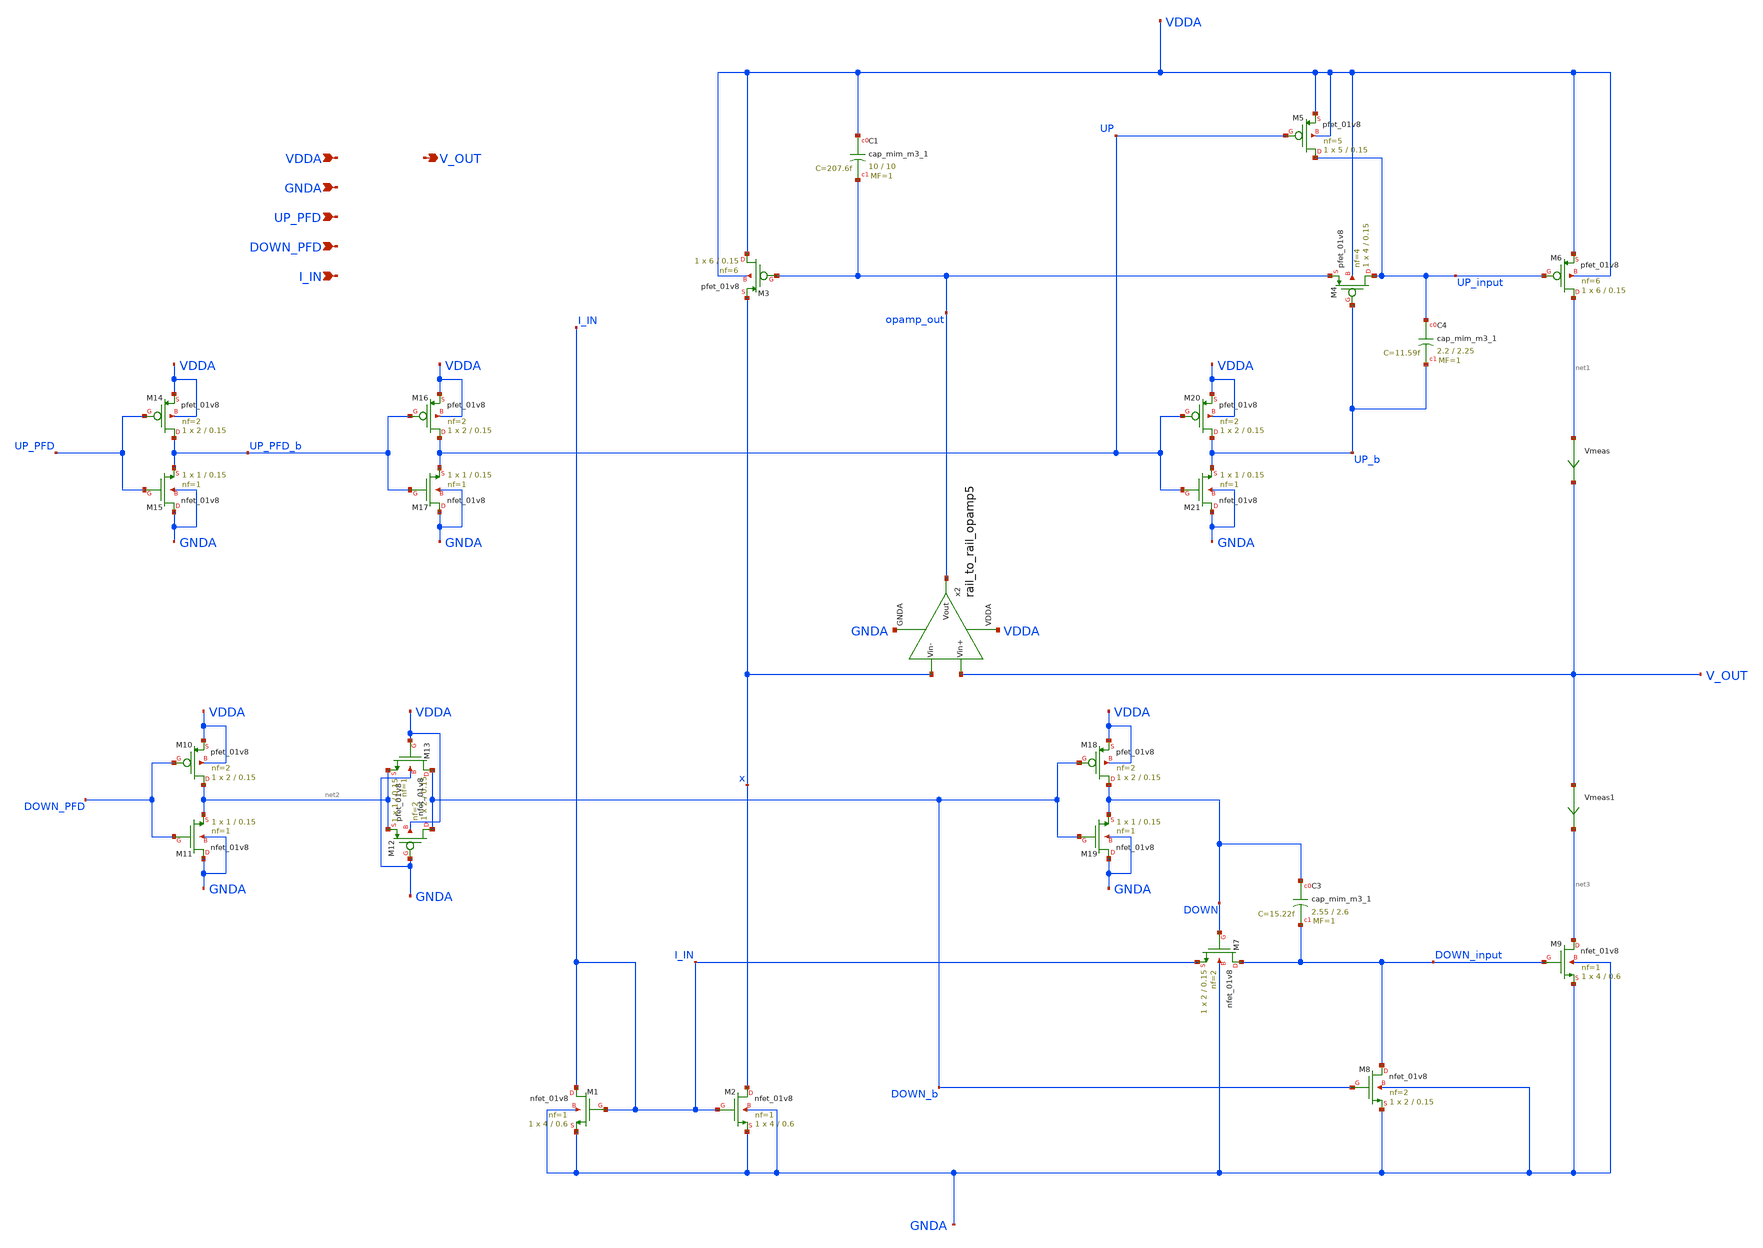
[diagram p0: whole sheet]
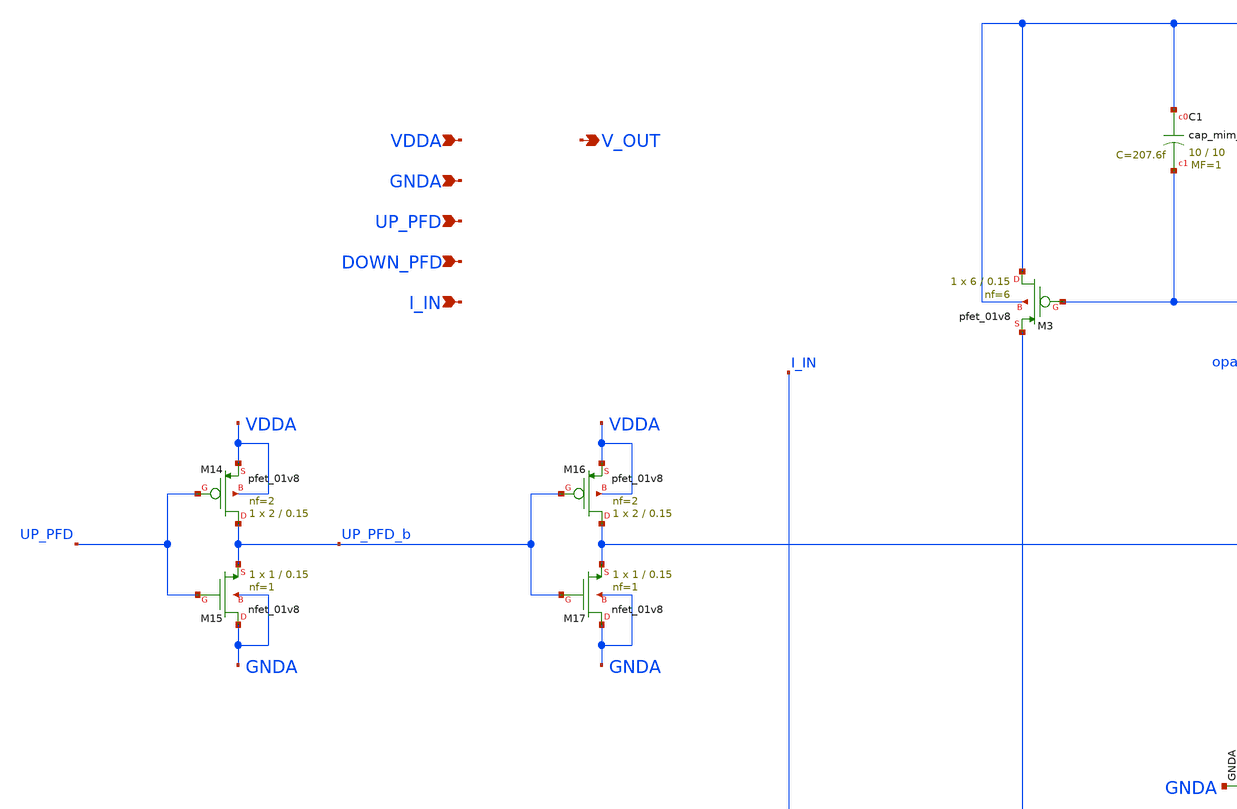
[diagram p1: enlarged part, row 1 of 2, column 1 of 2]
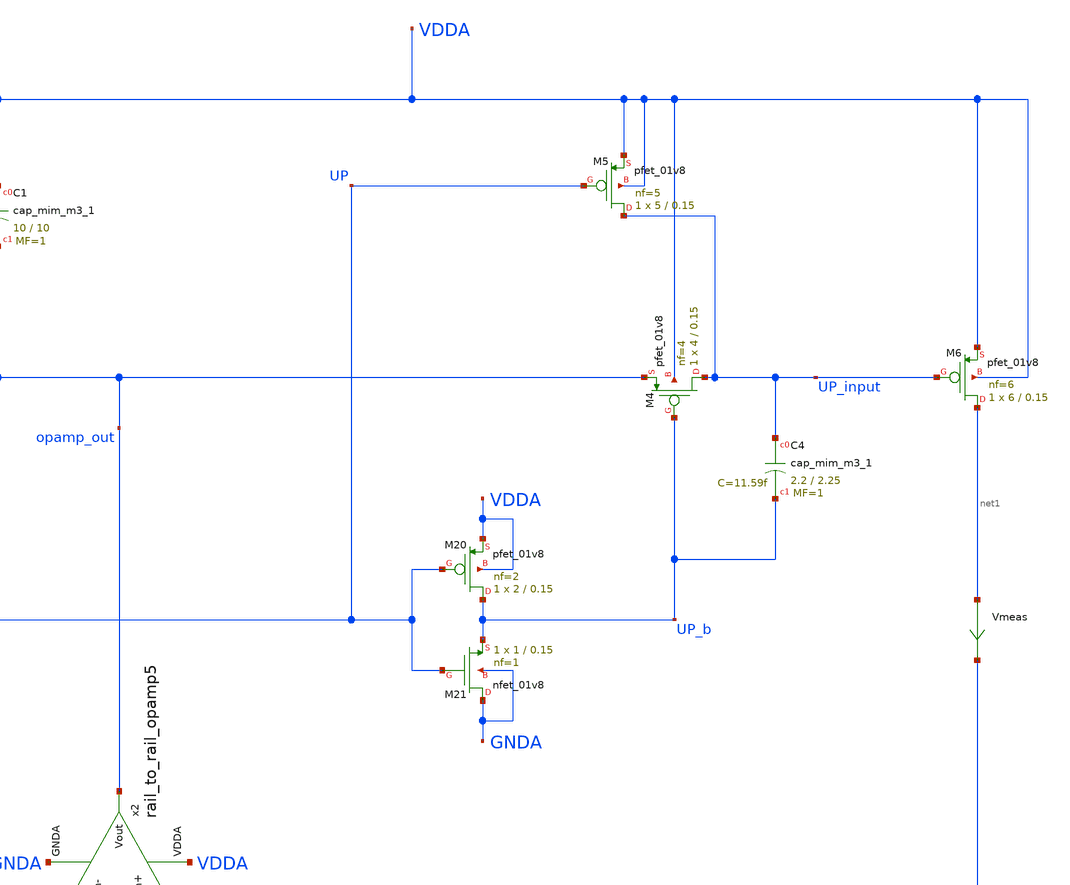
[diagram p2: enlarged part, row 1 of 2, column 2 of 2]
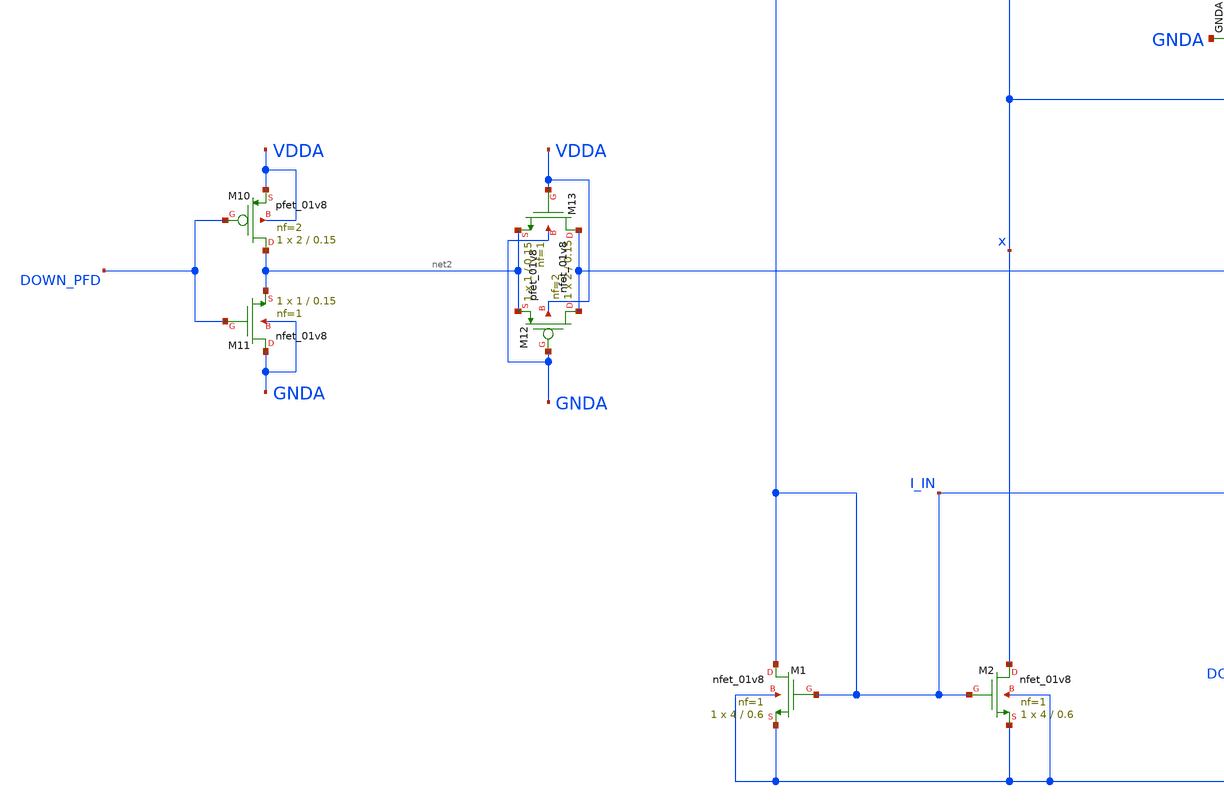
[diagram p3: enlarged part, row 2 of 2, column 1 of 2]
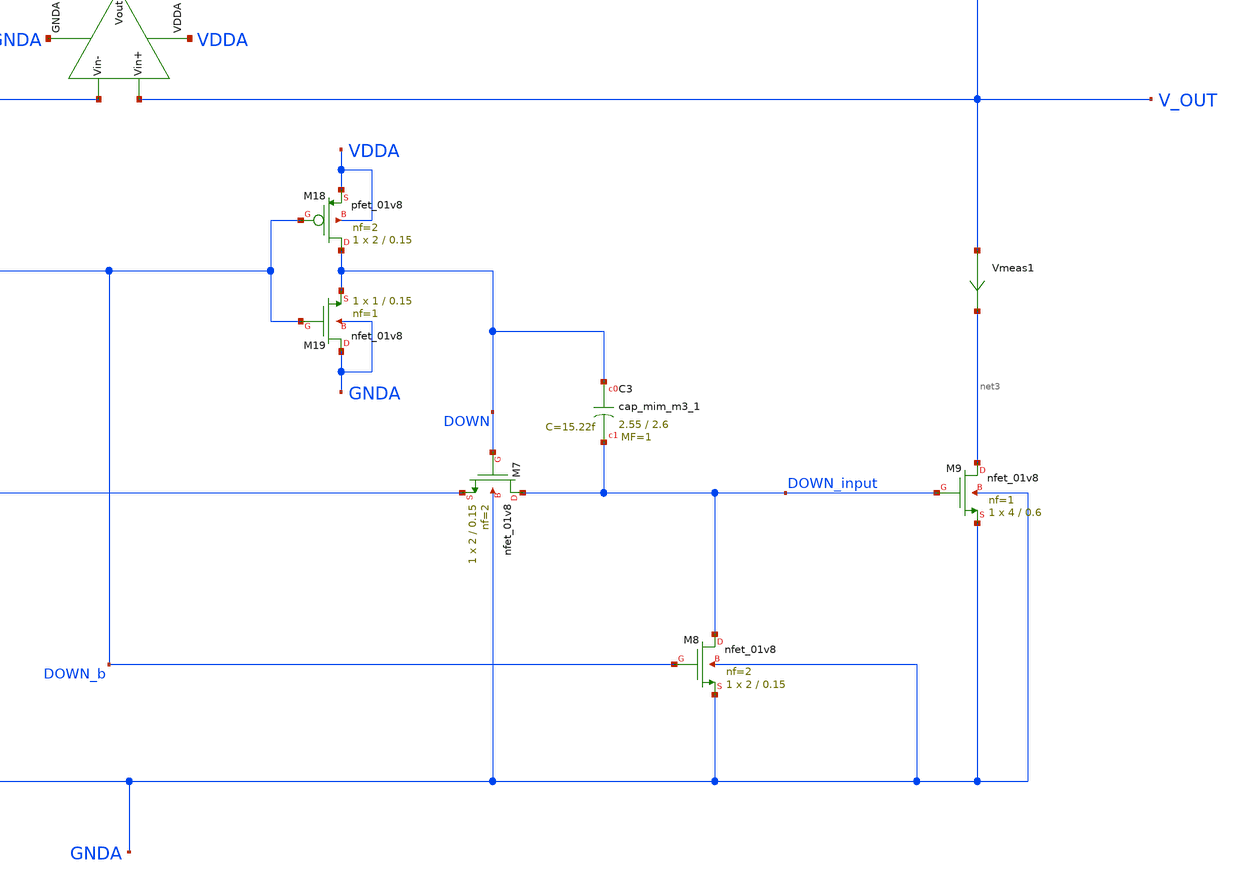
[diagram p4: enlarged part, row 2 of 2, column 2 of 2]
** sch_path: projects/pll/charge_pump/xschem_ngspice/charge_pump5.sch
**.subckt charge_pump5 VDDA V_OUT GNDA UP_PFD DOWN_PFD I_IN
*.ipin VDDA
*.opin V_OUT
*.ipin GNDA
*.ipin UP_PFD
*.ipin DOWN_PFD
*.ipin I_IN
XM1 I_IN I_IN GNDA GNDA sky130_fd_pr__nfet_01v8 L=0.6 W=4 nf=1 ad='int((nf+1)/2) * W/nf * 0.29' as='int((nf+2)/2) * W/nf * 0.29'
+ pd='2*int((nf+1)/2) * (W/nf + 0.29)' ps='2*int((nf+2)/2) * (W/nf + 0.29)' nrd='0.29 / W' nrs='0.29 / W'
+ sa=0 sb=0 sd=0 mult=1 m=1
XM2 x I_IN GNDA GNDA sky130_fd_pr__nfet_01v8 L=0.6 W=4 nf=1 ad='int((nf+1)/2) * W/nf * 0.29' as='int((nf+2)/2) * W/nf * 0.29'
+ pd='2*int((nf+1)/2) * (W/nf + 0.29)' ps='2*int((nf+2)/2) * (W/nf + 0.29)' nrd='0.29 / W' nrs='0.29 / W'
+ sa=0 sb=0 sd=0 mult=1 m=1
XM3 VDDA opamp_out x VDDA sky130_fd_pr__pfet_01v8 L=0.15 W=6 nf=6 ad='int((nf+1)/2) * W/nf * 0.29' as='int((nf+2)/2) * W/nf * 0.29'
+ pd='2*int((nf+1)/2) * (W/nf + 0.29)' ps='2*int((nf+2)/2) * (W/nf + 0.29)' nrd='0.29 / W' nrs='0.29 / W'
+ sa=0 sb=0 sd=0 mult=1 m=1
XM4 UP_input UP_b opamp_out VDDA sky130_fd_pr__pfet_01v8 L=0.15 W=4 nf=4 ad='int((nf+1)/2) * W/nf * 0.29'
+ as='int((nf+2)/2) * W/nf * 0.29' pd='2*int((nf+1)/2) * (W/nf + 0.29)' ps='2*int((nf+2)/2) * (W/nf + 0.29)'
+ nrd='0.29 / W' nrs='0.29 / W' sa=0 sb=0 sd=0 mult=1 m=1
XM5 UP_input UP VDDA VDDA sky130_fd_pr__pfet_01v8 L=0.15 W=5 nf=5 ad='int((nf+1)/2) * W/nf * 0.29' as='int((nf+2)/2) * W/nf * 0.29'
+ pd='2*int((nf+1)/2) * (W/nf + 0.29)' ps='2*int((nf+2)/2) * (W/nf + 0.29)' nrd='0.29 / W' nrs='0.29 / W'
+ sa=0 sb=0 sd=0 mult=1 m=1
XM6 net1 UP_input VDDA VDDA sky130_fd_pr__pfet_01v8 L=0.15 W=6 nf=6 ad='int((nf+1)/2) * W/nf * 0.29'
+ as='int((nf+2)/2) * W/nf * 0.29' pd='2*int((nf+1)/2) * (W/nf + 0.29)' ps='2*int((nf+2)/2) * (W/nf + 0.29)'
+ nrd='0.29 / W' nrs='0.29 / W' sa=0 sb=0 sd=0 mult=1 m=1
XM7 DOWN_input DOWN I_IN GNDA sky130_fd_pr__nfet_01v8 L=0.15 W=2 nf=2 ad='int((nf+1)/2) * W/nf * 0.29'
+ as='int((nf+2)/2) * W/nf * 0.29' pd='2*int((nf+1)/2) * (W/nf + 0.29)' ps='2*int((nf+2)/2) * (W/nf + 0.29)'
+ nrd='0.29 / W' nrs='0.29 / W' sa=0 sb=0 sd=0 mult=1 m=1
XM8 DOWN_input DOWN_b GNDA GNDA sky130_fd_pr__nfet_01v8 L=0.15 W=2 nf=2 ad='int((nf+1)/2) * W/nf * 0.29'
+ as='int((nf+2)/2) * W/nf * 0.29' pd='2*int((nf+1)/2) * (W/nf + 0.29)' ps='2*int((nf+2)/2) * (W/nf + 0.29)'
+ nrd='0.29 / W' nrs='0.29 / W' sa=0 sb=0 sd=0 mult=1 m=1
XM9 net3 DOWN_input GNDA GNDA sky130_fd_pr__nfet_01v8 L=0.6 W=4 nf=1 ad='int((nf+1)/2) * W/nf * 0.29'
+ as='int((nf+2)/2) * W/nf * 0.29' pd='2*int((nf+1)/2) * (W/nf + 0.29)' ps='2*int((nf+2)/2) * (W/nf + 0.29)'
+ nrd='0.29 / W' nrs='0.29 / W' sa=0 sb=0 sd=0 mult=1 m=1
x2 VDDA V_OUT x opamp_out GNDA rail_to_rail_opamp5
XM12 DOWN_b GNDA net2 VDDA sky130_fd_pr__pfet_01v8 L=0.15 W=2 nf=2 ad='int((nf+1)/2) * W/nf * 0.29' as='int((nf+2)/2) * W/nf * 0.29'
+ pd='2*int((nf+1)/2) * (W/nf + 0.29)' ps='2*int((nf+2)/2) * (W/nf + 0.29)' nrd='0.29 / W' nrs='0.29 / W'
+ sa=0 sb=0 sd=0 mult=1 m=1
XM13 DOWN_b VDDA net2 GNDA sky130_fd_pr__nfet_01v8 L=0.15 W=1 nf=1 ad='int((nf+1)/2) * W/nf * 0.29' as='int((nf+2)/2) * W/nf * 0.29'
+ pd='2*int((nf+1)/2) * (W/nf + 0.29)' ps='2*int((nf+2)/2) * (W/nf + 0.29)' nrd='0.29 / W' nrs='0.29 / W'
+ sa=0 sb=0 sd=0 mult=1 m=1
XC3 DOWN DOWN_input sky130_fd_pr__cap_mim_m3_1 W=2.55 L=2.6 MF=1 m=1
XC4 UP_input UP_b sky130_fd_pr__cap_mim_m3_1 W=2.2 L=2.25 MF=1 m=1
XM10 net2 DOWN_PFD VDDA VDDA sky130_fd_pr__pfet_01v8 L=0.15 W=2 nf=2 ad='int((nf+1)/2) * W/nf * 0.29'
+ as='int((nf+2)/2) * W/nf * 0.29' pd='2*int((nf+1)/2) * (W/nf + 0.29)' ps='2*int((nf+2)/2) * (W/nf + 0.29)'
+ nrd='0.29 / W' nrs='0.29 / W' sa=0 sb=0 sd=0 mult=1 m=1
XM11 GNDA DOWN_PFD net2 GNDA sky130_fd_pr__nfet_01v8 L=0.15 W=1 nf=1 ad='int((nf+1)/2) * W/nf * 0.29'
+ as='int((nf+2)/2) * W/nf * 0.29' pd='2*int((nf+1)/2) * (W/nf + 0.29)' ps='2*int((nf+2)/2) * (W/nf + 0.29)'
+ nrd='0.29 / W' nrs='0.29 / W' sa=0 sb=0 sd=0 mult=1 m=1
XM14 UP_PFD_b UP_PFD VDDA VDDA sky130_fd_pr__pfet_01v8 L=0.15 W=2 nf=2 ad='int((nf+1)/2) * W/nf * 0.29'
+ as='int((nf+2)/2) * W/nf * 0.29' pd='2*int((nf+1)/2) * (W/nf + 0.29)' ps='2*int((nf+2)/2) * (W/nf + 0.29)'
+ nrd='0.29 / W' nrs='0.29 / W' sa=0 sb=0 sd=0 mult=1 m=1
XM15 GNDA UP_PFD UP_PFD_b GNDA sky130_fd_pr__nfet_01v8 L=0.15 W=1 nf=1 ad='int((nf+1)/2) * W/nf * 0.29'
+ as='int((nf+2)/2) * W/nf * 0.29' pd='2*int((nf+1)/2) * (W/nf + 0.29)' ps='2*int((nf+2)/2) * (W/nf + 0.29)'
+ nrd='0.29 / W' nrs='0.29 / W' sa=0 sb=0 sd=0 mult=1 m=1
XM16 UP UP_PFD_b VDDA VDDA sky130_fd_pr__pfet_01v8 L=0.15 W=2 nf=2 ad='int((nf+1)/2) * W/nf * 0.29' as='int((nf+2)/2) * W/nf * 0.29'
+ pd='2*int((nf+1)/2) * (W/nf + 0.29)' ps='2*int((nf+2)/2) * (W/nf + 0.29)' nrd='0.29 / W' nrs='0.29 / W'
+ sa=0 sb=0 sd=0 mult=1 m=1
XM17 GNDA UP_PFD_b UP GNDA sky130_fd_pr__nfet_01v8 L=0.15 W=1 nf=1 ad='int((nf+1)/2) * W/nf * 0.29' as='int((nf+2)/2) * W/nf * 0.29'
+ pd='2*int((nf+1)/2) * (W/nf + 0.29)' ps='2*int((nf+2)/2) * (W/nf + 0.29)' nrd='0.29 / W' nrs='0.29 / W'
+ sa=0 sb=0 sd=0 mult=1 m=1
XM18 DOWN DOWN_b VDDA VDDA sky130_fd_pr__pfet_01v8 L=0.15 W=2 nf=2 ad='int((nf+1)/2) * W/nf * 0.29' as='int((nf+2)/2) * W/nf * 0.29'
+ pd='2*int((nf+1)/2) * (W/nf + 0.29)' ps='2*int((nf+2)/2) * (W/nf + 0.29)' nrd='0.29 / W' nrs='0.29 / W'
+ sa=0 sb=0 sd=0 mult=1 m=1
XM19 GNDA DOWN_b DOWN GNDA sky130_fd_pr__nfet_01v8 L=0.15 W=1 nf=1 ad='int((nf+1)/2) * W/nf * 0.29' as='int((nf+2)/2) * W/nf * 0.29'
+ pd='2*int((nf+1)/2) * (W/nf + 0.29)' ps='2*int((nf+2)/2) * (W/nf + 0.29)' nrd='0.29 / W' nrs='0.29 / W'
+ sa=0 sb=0 sd=0 mult=1 m=1
XM20 UP_b UP VDDA VDDA sky130_fd_pr__pfet_01v8 L=0.15 W=2 nf=2 ad='int((nf+1)/2) * W/nf * 0.29' as='int((nf+2)/2) * W/nf * 0.29'
+ pd='2*int((nf+1)/2) * (W/nf + 0.29)' ps='2*int((nf+2)/2) * (W/nf + 0.29)' nrd='0.29 / W' nrs='0.29 / W'
+ sa=0 sb=0 sd=0 mult=1 m=1
XM21 GNDA UP UP_b GNDA sky130_fd_pr__nfet_01v8 L=0.15 W=1 nf=1 ad='int((nf+1)/2) * W/nf * 0.29' as='int((nf+2)/2) * W/nf * 0.29'
+ pd='2*int((nf+1)/2) * (W/nf + 0.29)' ps='2*int((nf+2)/2) * (W/nf + 0.29)' nrd='0.29 / W' nrs='0.29 / W'
+ sa=0 sb=0 sd=0 mult=1 m=1
Vmeas net1 V_OUT 0
.save i(vmeas)
Vmeas1 V_OUT net3 0
.save i(vmeas1)
XC1 VDDA opamp_out sky130_fd_pr__cap_mim_m3_1 W=10 L=10 MF=1 m=1
**.ends

* expanding   symbol:
*+  /foss/designs/my_design/projects/pll/charge_pump/xschem_ngspice/rail_to_rail_opamp5.sym # of pins=5
** sym_path: projects/pll/charge_pump/xschem_ngspice/rail_to_rail_opamp5.sym
** sch_path: projects/pll/charge_pump/xschem_ngspice/rail_to_rail_opamp5.sch
.subckt rail_to_rail_opamp5 VDDA Vin+ Vin- Vout GNDA
*.opin Vout
*.ipin Vin+
*.ipin Vin-
*.ipin VDDA
*.ipin GNDA
XM2 n_left Vin+ v_common_n GNDA sky130_fd_pr__nfet_01v8 L=0.15 W=1 nf=1 ad='int((nf+1)/2) * W/nf * 0.29'
+ as='int((nf+2)/2) * W/nf * 0.29' pd='2*int((nf+1)/2) * (W/nf + 0.29)' ps='2*int((nf+2)/2) * (W/nf + 0.29)'
+ nrd='0.29 / W' nrs='0.29 / W' sa=0 sb=0 sd=0 mult=1 m=1
XM3 n_right Vin- v_common_n GNDA sky130_fd_pr__nfet_01v8 L=0.15 W=1 nf=1 ad='int((nf+1)/2) * W/nf * 0.29'
+ as='int((nf+2)/2) * W/nf * 0.29' pd='2*int((nf+1)/2) * (W/nf + 0.29)' ps='2*int((nf+2)/2) * (W/nf + 0.29)'
+ nrd='0.29 / W' nrs='0.29 / W' sa=0 sb=0 sd=0 mult=1 m=1
XM5 n_left n_left VDDA VDDA sky130_fd_pr__pfet_01v8 L=0.15 W=2 nf=2 ad='int((nf+1)/2) * W/nf * 0.29'
+ as='int((nf+2)/2) * W/nf * 0.29' pd='2*int((nf+1)/2) * (W/nf + 0.29)' ps='2*int((nf+2)/2) * (W/nf + 0.29)'
+ nrd='0.29 / W' nrs='0.29 / W' sa=0 sb=0 sd=0 mult=1 m=1
XM4 n_right n_left VDDA VDDA sky130_fd_pr__pfet_01v8 L=0.15 W=2 nf=2 ad='int((nf+1)/2) * W/nf * 0.29'
+ as='int((nf+2)/2) * W/nf * 0.29' pd='2*int((nf+1)/2) * (W/nf + 0.29)' ps='2*int((nf+2)/2) * (W/nf + 0.29)'
+ nrd='0.29 / W' nrs='0.29 / W' sa=0 sb=0 sd=0 mult=1 m=1
XM6 v_common_p p_bias VDDA VDDA sky130_fd_pr__pfet_01v8 L=0.15 W=3 nf=3 ad='int((nf+1)/2) * W/nf * 0.29'
+ as='int((nf+2)/2) * W/nf * 0.29' pd='2*int((nf+1)/2) * (W/nf + 0.29)' ps='2*int((nf+2)/2) * (W/nf + 0.29)'
+ nrd='0.29 / W' nrs='0.29 / W' sa=0 sb=0 sd=0 mult=1 m=1
XM7 p_left Vin+ v_common_p VDDA sky130_fd_pr__pfet_01v8 L=0.15 W=2 nf=2 ad='int((nf+1)/2) * W/nf * 0.29'
+ as='int((nf+2)/2) * W/nf * 0.29' pd='2*int((nf+1)/2) * (W/nf + 0.29)' ps='2*int((nf+2)/2) * (W/nf + 0.29)'
+ nrd='0.29 / W' nrs='0.29 / W' sa=0 sb=0 sd=0 mult=1 m=1
XM8 p_right Vin- v_common_p VDDA sky130_fd_pr__pfet_01v8 L=0.15 W=2 nf=2 ad='int((nf+1)/2) * W/nf * 0.29'
+ as='int((nf+2)/2) * W/nf * 0.29' pd='2*int((nf+1)/2) * (W/nf + 0.29)' ps='2*int((nf+2)/2) * (W/nf + 0.29)'
+ nrd='0.29 / W' nrs='0.29 / W' sa=0 sb=0 sd=0 mult=1 m=1
XM9 p_left p_left GNDA GNDA sky130_fd_pr__nfet_01v8 L=0.15 W=1 nf=1 ad='int((nf+1)/2) * W/nf * 0.29'
+ as='int((nf+2)/2) * W/nf * 0.29' pd='2*int((nf+1)/2) * (W/nf + 0.29)' ps='2*int((nf+2)/2) * (W/nf + 0.29)'
+ nrd='0.29 / W' nrs='0.29 / W' sa=0 sb=0 sd=0 mult=1 m=1
XM10 p_right p_left GNDA GNDA sky130_fd_pr__nfet_01v8 L=0.15 W=1 nf=1 ad='int((nf+1)/2) * W/nf * 0.29'
+ as='int((nf+2)/2) * W/nf * 0.29' pd='2*int((nf+1)/2) * (W/nf + 0.29)' ps='2*int((nf+2)/2) * (W/nf + 0.29)'
+ nrd='0.29 / W' nrs='0.29 / W' sa=0 sb=0 sd=0 mult=1 m=1
XM1 v_common_n n_bias GNDA GNDA sky130_fd_pr__nfet_01v8 L=0.15 W=1 nf=1 ad='int((nf+1)/2) * W/nf * 0.29'
+ as='int((nf+2)/2) * W/nf * 0.29' pd='2*int((nf+1)/2) * (W/nf + 0.29)' ps='2*int((nf+2)/2) * (W/nf + 0.29)'
+ nrd='0.29 / W' nrs='0.29 / W' sa=0 sb=0 sd=0 mult=1 m=1
XM11 Vout n_right VDDA VDDA sky130_fd_pr__pfet_01v8 L=0.15 W=2 nf=2 ad='int((nf+1)/2) * W/nf * 0.29'
+ as='int((nf+2)/2) * W/nf * 0.29' pd='2*int((nf+1)/2) * (W/nf + 0.29)' ps='2*int((nf+2)/2) * (W/nf + 0.29)'
+ nrd='0.29 / W' nrs='0.29 / W' sa=0 sb=0 sd=0 mult=1 m=1
XM12 Vout p_right GNDA GNDA sky130_fd_pr__nfet_01v8 L=0.15 W=1 nf=1 ad='int((nf+1)/2) * W/nf * 0.29'
+ as='int((nf+2)/2) * W/nf * 0.29' pd='2*int((nf+1)/2) * (W/nf + 0.29)' ps='2*int((nf+2)/2) * (W/nf + 0.29)'
+ nrd='0.29 / W' nrs='0.29 / W' sa=0 sb=0 sd=0 mult=1 m=1
XM13 n_bias n_bias GNDA GNDA sky130_fd_pr__nfet_01v8 L=0.15 W=1 nf=1 ad='int((nf+1)/2) * W/nf * 0.29'
+ as='int((nf+2)/2) * W/nf * 0.29' pd='2*int((nf+1)/2) * (W/nf + 0.29)' ps='2*int((nf+2)/2) * (W/nf + 0.29)'
+ nrd='0.29 / W' nrs='0.29 / W' sa=0 sb=0 sd=0 mult=1 m=1
XM15 p_bias p_bias VDDA VDDA sky130_fd_pr__pfet_01v8 L=0.15 W=2 nf=2 ad='int((nf+1)/2) * W/nf * 0.29'
+ as='int((nf+2)/2) * W/nf * 0.29' pd='2*int((nf+1)/2) * (W/nf + 0.29)' ps='2*int((nf+2)/2) * (W/nf + 0.29)'
+ nrd='0.29 / W' nrs='0.29 / W' sa=0 sb=0 sd=0 mult=1 m=1
Vmeas net1 n_bias 0
.save i(vmeas)
XM14 net1 net1 p_bias p_bias sky130_fd_pr__pfet_01v8 L=0.15 W=2 nf=2 ad='int((nf+1)/2) * W/nf * 0.29'
+ as='int((nf+2)/2) * W/nf * 0.29' pd='2*int((nf+1)/2) * (W/nf + 0.29)' ps='2*int((nf+2)/2) * (W/nf + 0.29)'
+ nrd='0.29 / W' nrs='0.29 / W' sa=0 sb=0 sd=0 mult=1 m=1
XC1 p_right GNDA sky130_fd_pr__cap_mim_m3_1 W=10 L=10 MF=1 m=1
XC2 VDDA n_right sky130_fd_pr__cap_mim_m3_1 W=10 L=10 MF=1 m=1
.ends

.end
